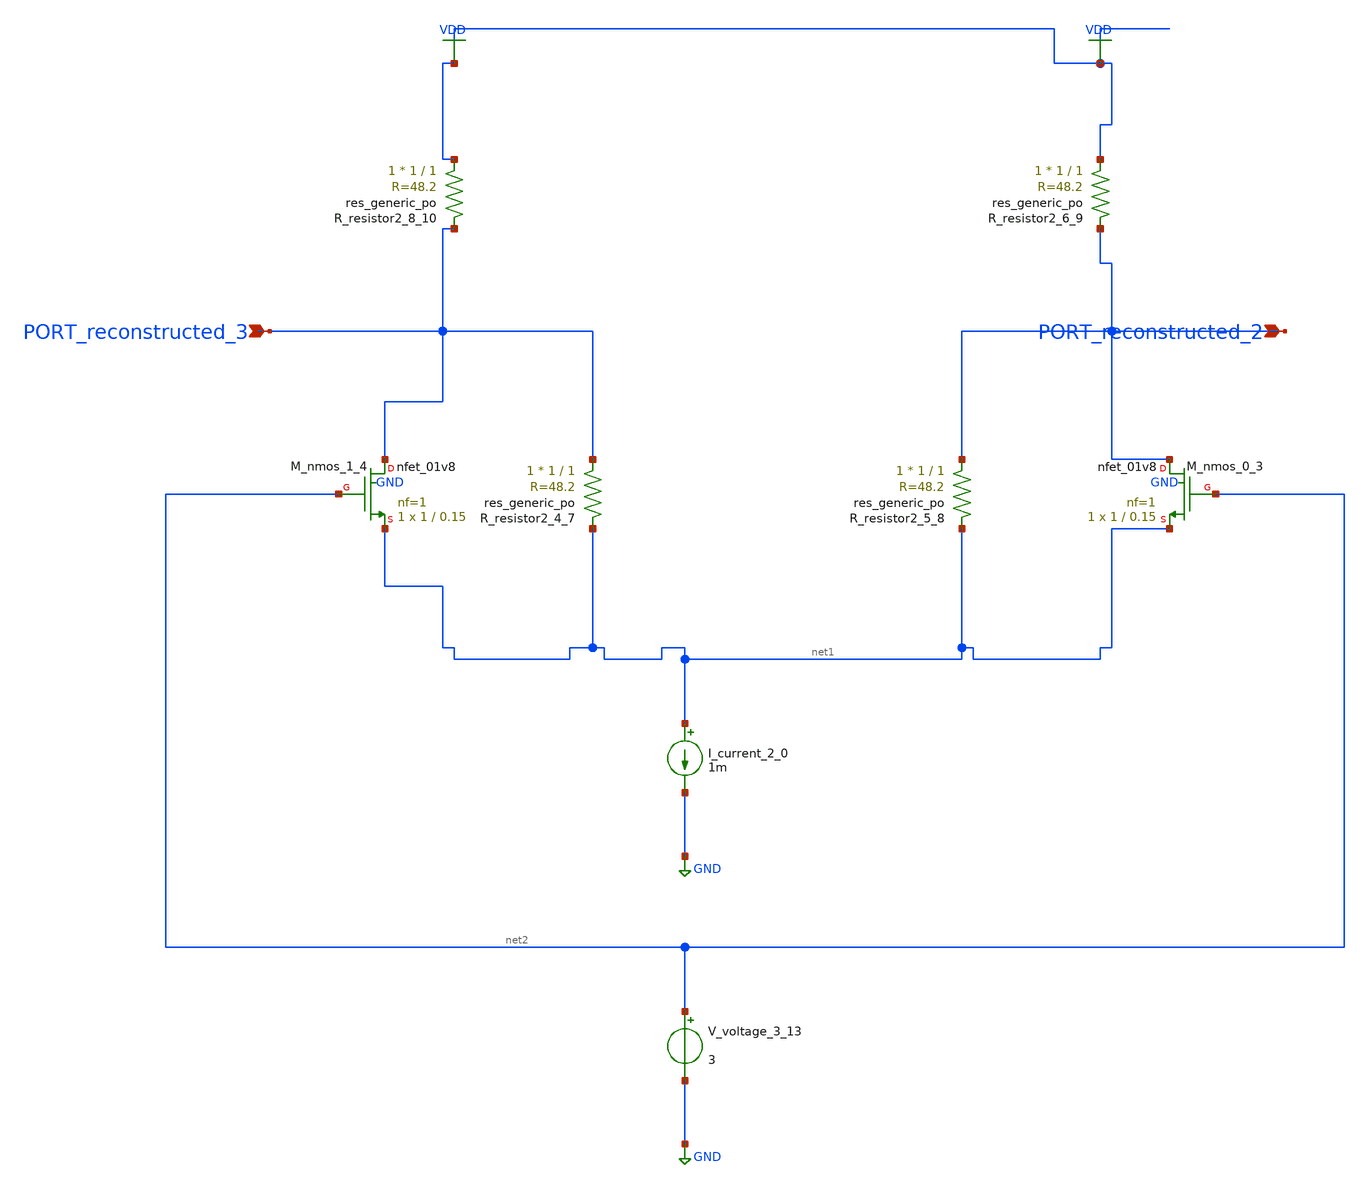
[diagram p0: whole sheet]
** sch_path: schematics/AMSNet/207.sch
**.subckt 207 PORT_reconstructed_2 PORT_reconstructed_3
*.ipin PORT_reconstructed_2
*.ipin PORT_reconstructed_3
I_current_2_0 net1 GND 1m
XM_nmos_0_3 PORT_reconstructed_2 net2 net1 GND sky130_fd_pr__nfet_01v8 L=0.15 W=1 nf=1 ad='int((1 + 1)/2) * 1 / 1 * 0.29'
+ as='int((1 + 2)/2) * 1 / 1 * 0.29' pd='2*int((1 + 1)/2) * (1 / 1 + 0.29)' ps='2*int((1 + 2)/2) * (1 / 1 + 0.29)'
+ nrd='0.29 / 1 ' nrs='0.29 / 1 ' sa=0 sb=0 sd=0 mult=1 m=1
XM_nmos_1_4 PORT_reconstructed_3 net2 net1 GND sky130_fd_pr__nfet_01v8 L=0.15 W=1 nf=1 ad='int((1 + 1)/2) * 1 / 1 * 0.29'
+ as='int((1 + 2)/2) * 1 / 1 * 0.29' pd='2*int((1 + 1)/2) * (1 / 1 + 0.29)' ps='2*int((1 + 2)/2) * (1 / 1 + 0.29)'
+ nrd='0.29 / 1 ' nrs='0.29 / 1 ' sa=0 sb=0 sd=0 mult=1 m=1
XR_resistor2_4_7 PORT_reconstructed_3 net1 sky130_fd_pr__res_generic_po W=1 L=1 m=1
XR_resistor2_5_8 PORT_reconstructed_2 net1 sky130_fd_pr__res_generic_po W=1 L=1 m=1
XR_resistor2_6_9 VDD PORT_reconstructed_2 sky130_fd_pr__res_generic_po W=1 L=1 m=1
XR_resistor2_8_10 VDD PORT_reconstructed_3 sky130_fd_pr__res_generic_po W=1 L=1 m=1
V_voltage_3_13 net2 GND 3
**.ends
.GLOBAL GND
.GLOBAL VDD
.end
